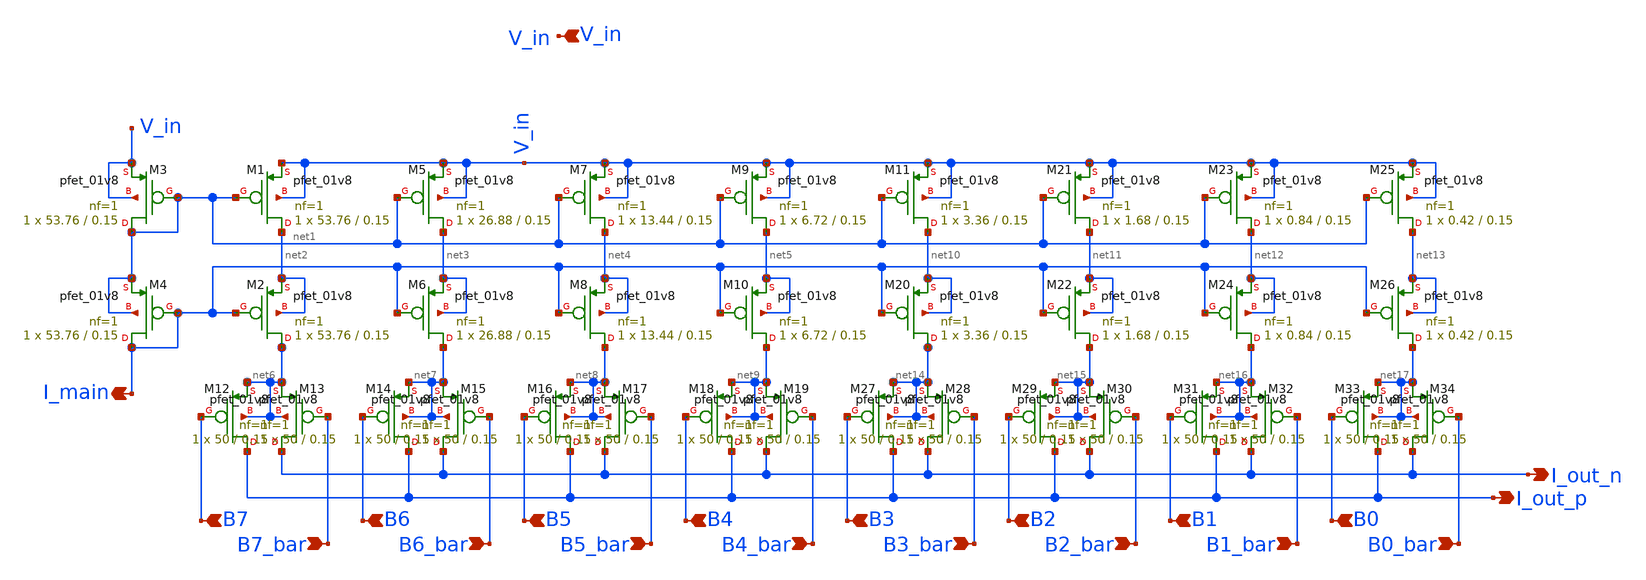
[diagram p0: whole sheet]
** sch_path: analog/schematics/DAC.sch
**.subckt DAC B0 B0_bar B1 B2 B3 B1_bar B2_bar B3_bar B4 B4_bar B5 B6 B7 B5_bar B6_bar B7_bar I_main
*+ I_out_p I_out_n V_in
*.ipin B0
*.ipin B0_bar
*.ipin B1
*.ipin B2
*.ipin B3
*.ipin B1_bar
*.ipin B2_bar
*.ipin B3_bar
*.ipin B4
*.ipin B4_bar
*.ipin B5
*.ipin B6
*.ipin B7
*.ipin B5_bar
*.ipin B6_bar
*.ipin B7_bar
*.opin I_main
*.opin I_out_p
*.opin I_out_n
*.ipin V_in
XM1 net2 net1 V_in V_in sky130_fd_pr__pfet_01v8 L=0.15 W=53.76 nf=1 ad='int((nf+1)/2) * W/nf * 0.29'
+ as='int((nf+2)/2) * W/nf * 0.29' pd='2*int((nf+1)/2) * (W/nf + 0.29)' ps='2*int((nf+2)/2) * (W/nf + 0.29)'
+ nrd='0.29 / W' nrs='0.29 / W' sa=0 sb=0 sd=0 mult=1 m=1
XM2 net6 I_main net2 net2 sky130_fd_pr__pfet_01v8 L=0.15 W=53.76 nf=1 ad='int((nf+1)/2) * W/nf * 0.29'
+ as='int((nf+2)/2) * W/nf * 0.29' pd='2*int((nf+1)/2) * (W/nf + 0.29)' ps='2*int((nf+2)/2) * (W/nf + 0.29)'
+ nrd='0.29 / W' nrs='0.29 / W' sa=0 sb=0 sd=0 mult=1 m=1
XM3 net1 net1 V_in V_in sky130_fd_pr__pfet_01v8 L=0.15 W=53.76 nf=1 ad='int((nf+1)/2) * W/nf * 0.29'
+ as='int((nf+2)/2) * W/nf * 0.29' pd='2*int((nf+1)/2) * (W/nf + 0.29)' ps='2*int((nf+2)/2) * (W/nf + 0.29)'
+ nrd='0.29 / W' nrs='0.29 / W' sa=0 sb=0 sd=0 mult=1 m=1
XM4 I_main I_main net1 net1 sky130_fd_pr__pfet_01v8 L=0.15 W=53.76 nf=1 ad='int((nf+1)/2) * W/nf * 0.29'
+ as='int((nf+2)/2) * W/nf * 0.29' pd='2*int((nf+1)/2) * (W/nf + 0.29)' ps='2*int((nf+2)/2) * (W/nf + 0.29)'
+ nrd='0.29 / W' nrs='0.29 / W' sa=0 sb=0 sd=0 mult=1 m=1
XM5 net3 net1 V_in V_in sky130_fd_pr__pfet_01v8 L=0.15 W=26.88 nf=1 ad='int((nf+1)/2) * W/nf * 0.29'
+ as='int((nf+2)/2) * W/nf * 0.29' pd='2*int((nf+1)/2) * (W/nf + 0.29)' ps='2*int((nf+2)/2) * (W/nf + 0.29)'
+ nrd='0.29 / W' nrs='0.29 / W' sa=0 sb=0 sd=0 mult=1 m=1
XM6 net7 I_main net3 net3 sky130_fd_pr__pfet_01v8 L=0.15 W=26.88 nf=1 ad='int((nf+1)/2) * W/nf * 0.29'
+ as='int((nf+2)/2) * W/nf * 0.29' pd='2*int((nf+1)/2) * (W/nf + 0.29)' ps='2*int((nf+2)/2) * (W/nf + 0.29)'
+ nrd='0.29 / W' nrs='0.29 / W' sa=0 sb=0 sd=0 mult=1 m=1
XM7 net4 net1 V_in V_in sky130_fd_pr__pfet_01v8 L=0.15 W=13.44 nf=1 ad='int((nf+1)/2) * W/nf * 0.29'
+ as='int((nf+2)/2) * W/nf * 0.29' pd='2*int((nf+1)/2) * (W/nf + 0.29)' ps='2*int((nf+2)/2) * (W/nf + 0.29)'
+ nrd='0.29 / W' nrs='0.29 / W' sa=0 sb=0 sd=0 mult=1 m=1
XM8 net8 I_main net4 net4 sky130_fd_pr__pfet_01v8 L=0.15 W=13.44 nf=1 ad='int((nf+1)/2) * W/nf * 0.29'
+ as='int((nf+2)/2) * W/nf * 0.29' pd='2*int((nf+1)/2) * (W/nf + 0.29)' ps='2*int((nf+2)/2) * (W/nf + 0.29)'
+ nrd='0.29 / W' nrs='0.29 / W' sa=0 sb=0 sd=0 mult=1 m=1
XM9 net5 net1 V_in V_in sky130_fd_pr__pfet_01v8 L=0.15 W=6.72 nf=1 ad='int((nf+1)/2) * W/nf * 0.29' as='int((nf+2)/2) * W/nf * 0.29'
+ pd='2*int((nf+1)/2) * (W/nf + 0.29)' ps='2*int((nf+2)/2) * (W/nf + 0.29)' nrd='0.29 / W' nrs='0.29 / W'
+ sa=0 sb=0 sd=0 mult=1 m=1
XM10 net9 I_main net5 net5 sky130_fd_pr__pfet_01v8 L=0.15 W=6.72 nf=1 ad='int((nf+1)/2) * W/nf * 0.29'
+ as='int((nf+2)/2) * W/nf * 0.29' pd='2*int((nf+1)/2) * (W/nf + 0.29)' ps='2*int((nf+2)/2) * (W/nf + 0.29)'
+ nrd='0.29 / W' nrs='0.29 / W' sa=0 sb=0 sd=0 mult=1 m=1
XM12 I_out_p B7 net6 net6 sky130_fd_pr__pfet_01v8 L=0.15 W=50 nf=1 ad='int((nf+1)/2) * W/nf * 0.29' as='int((nf+2)/2) * W/nf * 0.29'
+ pd='2*int((nf+1)/2) * (W/nf + 0.29)' ps='2*int((nf+2)/2) * (W/nf + 0.29)' nrd='0.29 / W' nrs='0.29 / W'
+ sa=0 sb=0 sd=0 mult=1 m=1
XM13 I_out_n B7_bar net6 net6 sky130_fd_pr__pfet_01v8 L=0.15 W=50 nf=1 ad='int((nf+1)/2) * W/nf * 0.29'
+ as='int((nf+2)/2) * W/nf * 0.29' pd='2*int((nf+1)/2) * (W/nf + 0.29)' ps='2*int((nf+2)/2) * (W/nf + 0.29)'
+ nrd='0.29 / W' nrs='0.29 / W' sa=0 sb=0 sd=0 mult=1 m=1
XM14 I_out_p B6 net7 net7 sky130_fd_pr__pfet_01v8 L=0.15 W=50 nf=1 ad='int((nf+1)/2) * W/nf * 0.29' as='int((nf+2)/2) * W/nf * 0.29'
+ pd='2*int((nf+1)/2) * (W/nf + 0.29)' ps='2*int((nf+2)/2) * (W/nf + 0.29)' nrd='0.29 / W' nrs='0.29 / W'
+ sa=0 sb=0 sd=0 mult=1 m=1
XM15 I_out_n B6_bar net7 net7 sky130_fd_pr__pfet_01v8 L=0.15 W=50 nf=1 ad='int((nf+1)/2) * W/nf * 0.29'
+ as='int((nf+2)/2) * W/nf * 0.29' pd='2*int((nf+1)/2) * (W/nf + 0.29)' ps='2*int((nf+2)/2) * (W/nf + 0.29)'
+ nrd='0.29 / W' nrs='0.29 / W' sa=0 sb=0 sd=0 mult=1 m=1
XM16 I_out_p B5 net8 net8 sky130_fd_pr__pfet_01v8 L=0.15 W=50 nf=1 ad='int((nf+1)/2) * W/nf * 0.29' as='int((nf+2)/2) * W/nf * 0.29'
+ pd='2*int((nf+1)/2) * (W/nf + 0.29)' ps='2*int((nf+2)/2) * (W/nf + 0.29)' nrd='0.29 / W' nrs='0.29 / W'
+ sa=0 sb=0 sd=0 mult=1 m=1
XM17 I_out_n B5_bar net8 net8 sky130_fd_pr__pfet_01v8 L=0.15 W=50 nf=1 ad='int((nf+1)/2) * W/nf * 0.29'
+ as='int((nf+2)/2) * W/nf * 0.29' pd='2*int((nf+1)/2) * (W/nf + 0.29)' ps='2*int((nf+2)/2) * (W/nf + 0.29)'
+ nrd='0.29 / W' nrs='0.29 / W' sa=0 sb=0 sd=0 mult=1 m=1
XM18 I_out_p B4 net9 net9 sky130_fd_pr__pfet_01v8 L=0.15 W=50 nf=1 ad='int((nf+1)/2) * W/nf * 0.29' as='int((nf+2)/2) * W/nf * 0.29'
+ pd='2*int((nf+1)/2) * (W/nf + 0.29)' ps='2*int((nf+2)/2) * (W/nf + 0.29)' nrd='0.29 / W' nrs='0.29 / W'
+ sa=0 sb=0 sd=0 mult=1 m=1
XM19 I_out_n B4_bar net9 net9 sky130_fd_pr__pfet_01v8 L=0.15 W=50 nf=1 ad='int((nf+1)/2) * W/nf * 0.29'
+ as='int((nf+2)/2) * W/nf * 0.29' pd='2*int((nf+1)/2) * (W/nf + 0.29)' ps='2*int((nf+2)/2) * (W/nf + 0.29)'
+ nrd='0.29 / W' nrs='0.29 / W' sa=0 sb=0 sd=0 mult=1 m=1
XM11 net10 net1 V_in V_in sky130_fd_pr__pfet_01v8 L=0.15 W=3.36 nf=1 ad='int((nf+1)/2) * W/nf * 0.29'
+ as='int((nf+2)/2) * W/nf * 0.29' pd='2*int((nf+1)/2) * (W/nf + 0.29)' ps='2*int((nf+2)/2) * (W/nf + 0.29)'
+ nrd='0.29 / W' nrs='0.29 / W' sa=0 sb=0 sd=0 mult=1 m=1
XM20 net14 I_main net10 net10 sky130_fd_pr__pfet_01v8 L=0.15 W=3.36 nf=1 ad='int((nf+1)/2) * W/nf * 0.29'
+ as='int((nf+2)/2) * W/nf * 0.29' pd='2*int((nf+1)/2) * (W/nf + 0.29)' ps='2*int((nf+2)/2) * (W/nf + 0.29)'
+ nrd='0.29 / W' nrs='0.29 / W' sa=0 sb=0 sd=0 mult=1 m=1
XM21 net11 net1 V_in V_in sky130_fd_pr__pfet_01v8 L=0.15 W=1.68 nf=1 ad='int((nf+1)/2) * W/nf * 0.29'
+ as='int((nf+2)/2) * W/nf * 0.29' pd='2*int((nf+1)/2) * (W/nf + 0.29)' ps='2*int((nf+2)/2) * (W/nf + 0.29)'
+ nrd='0.29 / W' nrs='0.29 / W' sa=0 sb=0 sd=0 mult=1 m=1
XM22 net15 I_main net11 net11 sky130_fd_pr__pfet_01v8 L=0.15 W=1.68 nf=1 ad='int((nf+1)/2) * W/nf * 0.29'
+ as='int((nf+2)/2) * W/nf * 0.29' pd='2*int((nf+1)/2) * (W/nf + 0.29)' ps='2*int((nf+2)/2) * (W/nf + 0.29)'
+ nrd='0.29 / W' nrs='0.29 / W' sa=0 sb=0 sd=0 mult=1 m=1
XM23 net12 net1 V_in V_in sky130_fd_pr__pfet_01v8 L=0.15 W=0.84 nf=1 ad='int((nf+1)/2) * W/nf * 0.29'
+ as='int((nf+2)/2) * W/nf * 0.29' pd='2*int((nf+1)/2) * (W/nf + 0.29)' ps='2*int((nf+2)/2) * (W/nf + 0.29)'
+ nrd='0.29 / W' nrs='0.29 / W' sa=0 sb=0 sd=0 mult=1 m=1
XM24 net16 I_main net12 net12 sky130_fd_pr__pfet_01v8 L=0.15 W=0.84 nf=1 ad='int((nf+1)/2) * W/nf * 0.29'
+ as='int((nf+2)/2) * W/nf * 0.29' pd='2*int((nf+1)/2) * (W/nf + 0.29)' ps='2*int((nf+2)/2) * (W/nf + 0.29)'
+ nrd='0.29 / W' nrs='0.29 / W' sa=0 sb=0 sd=0 mult=1 m=1
XM25 net13 net1 V_in V_in sky130_fd_pr__pfet_01v8 L=0.15 W=0.42 nf=1 ad='int((nf+1)/2) * W/nf * 0.29'
+ as='int((nf+2)/2) * W/nf * 0.29' pd='2*int((nf+1)/2) * (W/nf + 0.29)' ps='2*int((nf+2)/2) * (W/nf + 0.29)'
+ nrd='0.29 / W' nrs='0.29 / W' sa=0 sb=0 sd=0 mult=1 m=1
XM26 net17 I_main net13 net13 sky130_fd_pr__pfet_01v8 L=0.15 W=0.42 nf=1 ad='int((nf+1)/2) * W/nf * 0.29'
+ as='int((nf+2)/2) * W/nf * 0.29' pd='2*int((nf+1)/2) * (W/nf + 0.29)' ps='2*int((nf+2)/2) * (W/nf + 0.29)'
+ nrd='0.29 / W' nrs='0.29 / W' sa=0 sb=0 sd=0 mult=1 m=1
XM27 I_out_p B3 net14 net14 sky130_fd_pr__pfet_01v8 L=0.15 W=50 nf=1 ad='int((nf+1)/2) * W/nf * 0.29'
+ as='int((nf+2)/2) * W/nf * 0.29' pd='2*int((nf+1)/2) * (W/nf + 0.29)' ps='2*int((nf+2)/2) * (W/nf + 0.29)'
+ nrd='0.29 / W' nrs='0.29 / W' sa=0 sb=0 sd=0 mult=1 m=1
XM28 I_out_n B3_bar net14 net14 sky130_fd_pr__pfet_01v8 L=0.15 W=50 nf=1 ad='int((nf+1)/2) * W/nf * 0.29'
+ as='int((nf+2)/2) * W/nf * 0.29' pd='2*int((nf+1)/2) * (W/nf + 0.29)' ps='2*int((nf+2)/2) * (W/nf + 0.29)'
+ nrd='0.29 / W' nrs='0.29 / W' sa=0 sb=0 sd=0 mult=1 m=1
XM29 I_out_p B2 net15 net15 sky130_fd_pr__pfet_01v8 L=0.15 W=50 nf=1 ad='int((nf+1)/2) * W/nf * 0.29'
+ as='int((nf+2)/2) * W/nf * 0.29' pd='2*int((nf+1)/2) * (W/nf + 0.29)' ps='2*int((nf+2)/2) * (W/nf + 0.29)'
+ nrd='0.29 / W' nrs='0.29 / W' sa=0 sb=0 sd=0 mult=1 m=1
XM30 I_out_n B2_bar net15 net15 sky130_fd_pr__pfet_01v8 L=0.15 W=50 nf=1 ad='int((nf+1)/2) * W/nf * 0.29'
+ as='int((nf+2)/2) * W/nf * 0.29' pd='2*int((nf+1)/2) * (W/nf + 0.29)' ps='2*int((nf+2)/2) * (W/nf + 0.29)'
+ nrd='0.29 / W' nrs='0.29 / W' sa=0 sb=0 sd=0 mult=1 m=1
XM31 I_out_p B1 net16 net16 sky130_fd_pr__pfet_01v8 L=0.15 W=50 nf=1 ad='int((nf+1)/2) * W/nf * 0.29'
+ as='int((nf+2)/2) * W/nf * 0.29' pd='2*int((nf+1)/2) * (W/nf + 0.29)' ps='2*int((nf+2)/2) * (W/nf + 0.29)'
+ nrd='0.29 / W' nrs='0.29 / W' sa=0 sb=0 sd=0 mult=1 m=1
XM32 I_out_n B1_bar net16 net16 sky130_fd_pr__pfet_01v8 L=0.15 W=50 nf=1 ad='int((nf+1)/2) * W/nf * 0.29'
+ as='int((nf+2)/2) * W/nf * 0.29' pd='2*int((nf+1)/2) * (W/nf + 0.29)' ps='2*int((nf+2)/2) * (W/nf + 0.29)'
+ nrd='0.29 / W' nrs='0.29 / W' sa=0 sb=0 sd=0 mult=1 m=1
XM33 I_out_p B0 net17 net17 sky130_fd_pr__pfet_01v8 L=0.15 W=50 nf=1 ad='int((nf+1)/2) * W/nf * 0.29'
+ as='int((nf+2)/2) * W/nf * 0.29' pd='2*int((nf+1)/2) * (W/nf + 0.29)' ps='2*int((nf+2)/2) * (W/nf + 0.29)'
+ nrd='0.29 / W' nrs='0.29 / W' sa=0 sb=0 sd=0 mult=1 m=1
XM34 I_out_n B0_bar net17 net17 sky130_fd_pr__pfet_01v8 L=0.15 W=50 nf=1 ad='int((nf+1)/2) * W/nf * 0.29'
+ as='int((nf+2)/2) * W/nf * 0.29' pd='2*int((nf+1)/2) * (W/nf + 0.29)' ps='2*int((nf+2)/2) * (W/nf + 0.29)'
+ nrd='0.29 / W' nrs='0.29 / W' sa=0 sb=0 sd=0 mult=1 m=1
**.ends
.end
